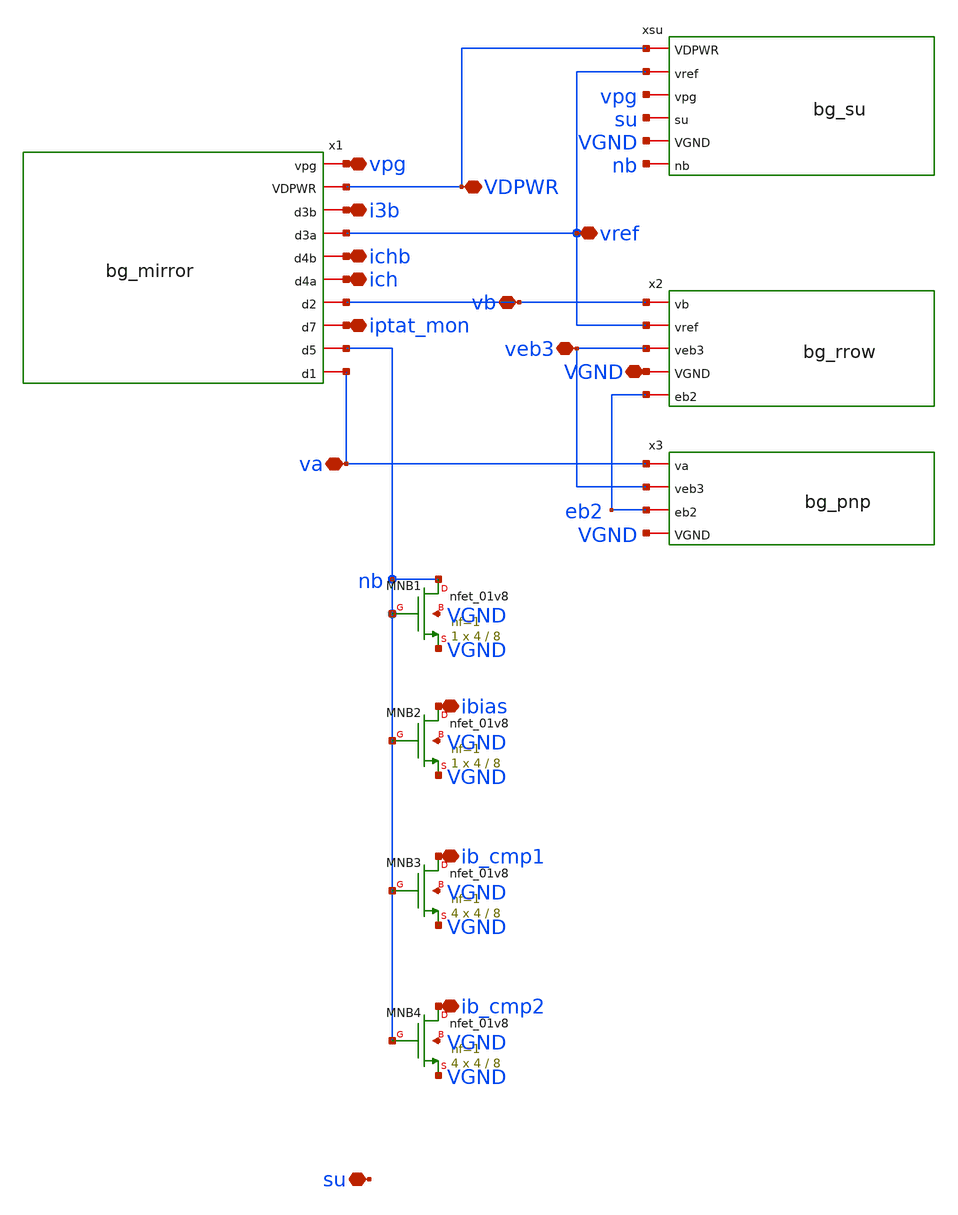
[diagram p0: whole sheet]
** sch_path: xschem/bg_core.sch
**.subckt bg_core va vb vref veb3 vpg i3b VDPWR ichb ich iptat_mon ibias ib_cmp1 ib_cmp2 VGND su
*.iopin va
*.iopin vb
*.iopin vref
*.iopin veb3
*.iopin vpg
*.iopin i3b
*.iopin VDPWR
*.iopin ichb
*.iopin ich
*.iopin iptat_mon
*.iopin ibias
*.iopin ib_cmp1
*.iopin ib_cmp2
*.iopin VGND
*.iopin su
x1 vpg VDPWR i3b vref ichb ich vb iptat_mon nb va bg_mirror
x2 vb vref veb3 VGND eb2 bg_rrow
x3 va veb3 eb2 VGND bg_pnp
XMNB1 nb nb VGND VGND sky130_fd_pr__nfet_01v8 L=8 W=4 nf=1 ad='int((1 + 1)/2) * 4 / 1 * 0.29' as='int((1 + 2)/2) * 4 / 1 * 0.29'
+ pd='2*int((1 + 1)/2) * (4 / 1 + 0.29)' ps='2*int((1 + 2)/2) * (4 / 1 + 0.29)' nrd='0.29 / 4 ' nrs='0.29 / 4 '
+ sa=0 sb=0 sd=0 mult=1 m=1
XMNB2 ibias nb VGND VGND sky130_fd_pr__nfet_01v8 L=8 W=4 nf=1 ad='int((1 + 1)/2) * 4 / 1 * 0.29' as='int((1 + 2)/2) * 4 / 1 * 0.29'
+ pd='2*int((1 + 1)/2) * (4 / 1 + 0.29)' ps='2*int((1 + 2)/2) * (4 / 1 + 0.29)' nrd='0.29 / 4 ' nrs='0.29 / 4 '
+ sa=0 sb=0 sd=0 mult=1 m=1
XMNB3 ib_cmp1 nb VGND VGND sky130_fd_pr__nfet_01v8 L=8 W=4 nf=1 ad='int((1 + 1)/2) * 4 / 1 * 0.29' as='int((1 + 2)/2) * 4 / 1 * 0.29'
+ pd='2*int((1 + 1)/2) * (4 / 1 + 0.29)' ps='2*int((1 + 2)/2) * (4 / 1 + 0.29)' nrd='0.29 / 4 ' nrs='0.29 / 4 '
+ sa=0 sb=0 sd=0 mult=4 m=4
XMNB4 ib_cmp2 nb VGND VGND sky130_fd_pr__nfet_01v8 L=8 W=4 nf=1 ad='int((1 + 1)/2) * 4 / 1 * 0.29' as='int((1 + 2)/2) * 4 / 1 * 0.29'
+ pd='2*int((1 + 1)/2) * (4 / 1 + 0.29)' ps='2*int((1 + 2)/2) * (4 / 1 + 0.29)' nrd='0.29 / 4 ' nrs='0.29 / 4 '
+ sa=0 sb=0 sd=0 mult=4 m=4
xsu VDPWR vref vpg su VGND nb bg_su
**.ends

* expanding   symbol:  bg_mirror.sym # of pins=10
** sym_path: xschem/bg_mirror.sym
** sch_path: xschem/bg_mirror.sch
.subckt bg_mirror vpg VDPWR d3b d3a d4b d4a d2 d7 d5 d1
*.iopin vpg
*.iopin VDPWR
*.iopin d1
*.iopin d2
*.iopin d3a
*.iopin d3b
*.iopin d4a
*.iopin d4b
*.iopin d7
*.iopin d5
XMP1 d1 vpg VDPWR VDPWR sky130_fd_pr__pfet_01v8 L=20 W=8.8 nf=1 ad='int((1 + 1)/2) * 8.8 / 1 * 0.29'
+ as='int((1 + 2)/2) * 8.8 / 1 * 0.29' pd='2*int((1 + 1)/2) * (8.8 / 1 + 0.29)' ps='2*int((1 + 2)/2) * (8.8 / 1 + 0.29)'
+ nrd='0.29 / 8.8 ' nrs='0.29 / 8.8 ' sa=0 sb=0 sd=0 mult=4 m=4
XMP2 d2 vpg VDPWR VDPWR sky130_fd_pr__pfet_01v8 L=20 W=8.8 nf=1 ad='int((1 + 1)/2) * 8.8 / 1 * 0.29'
+ as='int((1 + 2)/2) * 8.8 / 1 * 0.29' pd='2*int((1 + 1)/2) * (8.8 / 1 + 0.29)' ps='2*int((1 + 2)/2) * (8.8 / 1 + 0.29)'
+ nrd='0.29 / 8.8 ' nrs='0.29 / 8.8 ' sa=0 sb=0 sd=0 mult=4 m=4
XMP3A d3a vpg VDPWR VDPWR sky130_fd_pr__pfet_01v8 L=20 W=8.8 nf=1 ad='int((1 + 1)/2) * 8.8 / 1 * 0.29'
+ as='int((1 + 2)/2) * 8.8 / 1 * 0.29' pd='2*int((1 + 1)/2) * (8.8 / 1 + 0.29)' ps='2*int((1 + 2)/2) * (8.8 / 1 + 0.29)'
+ nrd='0.29 / 8.8 ' nrs='0.29 / 8.8 ' sa=0 sb=0 sd=0 mult=2 m=2
XMP3B d3b vpg VDPWR VDPWR sky130_fd_pr__pfet_01v8 L=20 W=8.8 nf=1 ad='int((1 + 1)/2) * 8.8 / 1 * 0.29'
+ as='int((1 + 2)/2) * 8.8 / 1 * 0.29' pd='2*int((1 + 1)/2) * (8.8 / 1 + 0.29)' ps='2*int((1 + 2)/2) * (8.8 / 1 + 0.29)'
+ nrd='0.29 / 8.8 ' nrs='0.29 / 8.8 ' sa=0 sb=0 sd=0 mult=2 m=2
XMP4A d4a vpg VDPWR VDPWR sky130_fd_pr__pfet_01v8 L=20 W=8.8 nf=1 ad='int((1 + 1)/2) * 8.8 / 1 * 0.29'
+ as='int((1 + 2)/2) * 8.8 / 1 * 0.29' pd='2*int((1 + 1)/2) * (8.8 / 1 + 0.29)' ps='2*int((1 + 2)/2) * (8.8 / 1 + 0.29)'
+ nrd='0.29 / 8.8 ' nrs='0.29 / 8.8 ' sa=0 sb=0 sd=0 mult=1 m=1
XMP4B d4b vpg VDPWR VDPWR sky130_fd_pr__pfet_01v8 L=20 W=8.8 nf=1 ad='int((1 + 1)/2) * 8.8 / 1 * 0.29'
+ as='int((1 + 2)/2) * 8.8 / 1 * 0.29' pd='2*int((1 + 1)/2) * (8.8 / 1 + 0.29)' ps='2*int((1 + 2)/2) * (8.8 / 1 + 0.29)'
+ nrd='0.29 / 8.8 ' nrs='0.29 / 8.8 ' sa=0 sb=0 sd=0 mult=1 m=1
XMP7 d7 vpg VDPWR VDPWR sky130_fd_pr__pfet_01v8 L=20 W=8.8 nf=1 ad='int((1 + 1)/2) * 8.8 / 1 * 0.29'
+ as='int((1 + 2)/2) * 8.8 / 1 * 0.29' pd='2*int((1 + 1)/2) * (8.8 / 1 + 0.29)' ps='2*int((1 + 2)/2) * (8.8 / 1 + 0.29)'
+ nrd='0.29 / 8.8 ' nrs='0.29 / 8.8 ' sa=0 sb=0 sd=0 mult=2 m=2
XMP5 d5 vpg VDPWR VDPWR sky130_fd_pr__pfet_01v8 L=20 W=8.8 nf=1 ad='int((1 + 1)/2) * 8.8 / 1 * 0.29'
+ as='int((1 + 2)/2) * 8.8 / 1 * 0.29' pd='2*int((1 + 1)/2) * (8.8 / 1 + 0.29)' ps='2*int((1 + 2)/2) * (8.8 / 1 + 0.29)'
+ nrd='0.29 / 8.8 ' nrs='0.29 / 8.8 ' sa=0 sb=0 sd=0 mult=2 m=2
.ends


* expanding   symbol:  bg_rrow.sym # of pins=5
** sym_path: xschem/bg_rrow.sym
** sch_path: xschem/bg_rrow.sch
.subckt bg_rrow vb vref veb3 VGND eb2
*.iopin vb
*.iopin eb2
*.iopin vref
*.iopin veb3
*.iopin VGND
XR1_1 eb2 net1 VGND sky130_fd_pr__res_high_po_1p41 L=20 mult=1 m=1
XR1_2 net1 net2 VGND sky130_fd_pr__res_high_po_1p41 L=20 mult=1 m=1
XR1_3 net2 net3 VGND sky130_fd_pr__res_high_po_1p41 L=20 mult=1 m=1
XR1_4 net3 vb VGND sky130_fd_pr__res_high_po_1p41 L=20 mult=1 m=1
XR3[39] r3n[38] vref VGND sky130_fd_pr__res_high_po_1p41 L=20 mult=1 m=1
XR3[38] r3n[37] r3n[38] VGND sky130_fd_pr__res_high_po_1p41 L=20 mult=1 m=1
XR3[37] r3n[36] r3n[37] VGND sky130_fd_pr__res_high_po_1p41 L=20 mult=1 m=1
XR3[36] r3n[35] r3n[36] VGND sky130_fd_pr__res_high_po_1p41 L=20 mult=1 m=1
XR3[35] r3n[34] r3n[35] VGND sky130_fd_pr__res_high_po_1p41 L=20 mult=1 m=1
XR3[34] r3n[33] r3n[34] VGND sky130_fd_pr__res_high_po_1p41 L=20 mult=1 m=1
XR3[33] r3n[32] r3n[33] VGND sky130_fd_pr__res_high_po_1p41 L=20 mult=1 m=1
XR3[32] r3n[31] r3n[32] VGND sky130_fd_pr__res_high_po_1p41 L=20 mult=1 m=1
XR3[31] r3n[30] r3n[31] VGND sky130_fd_pr__res_high_po_1p41 L=20 mult=1 m=1
XR3[30] r3n[29] r3n[30] VGND sky130_fd_pr__res_high_po_1p41 L=20 mult=1 m=1
XR3[29] r3n[28] r3n[29] VGND sky130_fd_pr__res_high_po_1p41 L=20 mult=1 m=1
XR3[28] r3n[27] r3n[28] VGND sky130_fd_pr__res_high_po_1p41 L=20 mult=1 m=1
XR3[27] r3n[26] r3n[27] VGND sky130_fd_pr__res_high_po_1p41 L=20 mult=1 m=1
XR3[26] r3n[25] r3n[26] VGND sky130_fd_pr__res_high_po_1p41 L=20 mult=1 m=1
XR3[25] r3n[24] r3n[25] VGND sky130_fd_pr__res_high_po_1p41 L=20 mult=1 m=1
XR3[24] r3n[23] r3n[24] VGND sky130_fd_pr__res_high_po_1p41 L=20 mult=1 m=1
XR3[23] r3n[22] r3n[23] VGND sky130_fd_pr__res_high_po_1p41 L=20 mult=1 m=1
XR3[22] r3n[21] r3n[22] VGND sky130_fd_pr__res_high_po_1p41 L=20 mult=1 m=1
XR3[21] r3n[20] r3n[21] VGND sky130_fd_pr__res_high_po_1p41 L=20 mult=1 m=1
XR3[20] r3n[19] r3n[20] VGND sky130_fd_pr__res_high_po_1p41 L=20 mult=1 m=1
XR3[19] r3n[18] r3n[19] VGND sky130_fd_pr__res_high_po_1p41 L=20 mult=1 m=1
XR3[18] r3n[17] r3n[18] VGND sky130_fd_pr__res_high_po_1p41 L=20 mult=1 m=1
XR3[17] r3n[16] r3n[17] VGND sky130_fd_pr__res_high_po_1p41 L=20 mult=1 m=1
XR3[16] r3n[15] r3n[16] VGND sky130_fd_pr__res_high_po_1p41 L=20 mult=1 m=1
XR3[15] r3n[14] r3n[15] VGND sky130_fd_pr__res_high_po_1p41 L=20 mult=1 m=1
XR3[14] r3n[13] r3n[14] VGND sky130_fd_pr__res_high_po_1p41 L=20 mult=1 m=1
XR3[13] r3n[12] r3n[13] VGND sky130_fd_pr__res_high_po_1p41 L=20 mult=1 m=1
XR3[12] r3n[11] r3n[12] VGND sky130_fd_pr__res_high_po_1p41 L=20 mult=1 m=1
XR3[11] r3n[10] r3n[11] VGND sky130_fd_pr__res_high_po_1p41 L=20 mult=1 m=1
XR3[10] r3n[9] r3n[10] VGND sky130_fd_pr__res_high_po_1p41 L=20 mult=1 m=1
XR3[9] r3n[8] r3n[9] VGND sky130_fd_pr__res_high_po_1p41 L=20 mult=1 m=1
XR3[8] r3n[7] r3n[8] VGND sky130_fd_pr__res_high_po_1p41 L=20 mult=1 m=1
XR3[7] r3n[6] r3n[7] VGND sky130_fd_pr__res_high_po_1p41 L=20 mult=1 m=1
XR3[6] r3n[5] r3n[6] VGND sky130_fd_pr__res_high_po_1p41 L=20 mult=1 m=1
XR3[5] r3n[4] r3n[5] VGND sky130_fd_pr__res_high_po_1p41 L=20 mult=1 m=1
XR3[4] r3n[3] r3n[4] VGND sky130_fd_pr__res_high_po_1p41 L=20 mult=1 m=1
XR3[3] r3n[2] r3n[3] VGND sky130_fd_pr__res_high_po_1p41 L=20 mult=1 m=1
XR3[2] r3n[1] r3n[2] VGND sky130_fd_pr__res_high_po_1p41 L=20 mult=1 m=1
XR3[1] r3n[0] r3n[1] VGND sky130_fd_pr__res_high_po_1p41 L=20 mult=1 m=1
XR3[0] veb3 r3n[0] VGND sky130_fd_pr__res_high_po_1p41 L=20 mult=1 m=1
XRD[3] VGND VGND VGND sky130_fd_pr__res_high_po_1p41 L=20 mult=1 m=1
XRD[2] VGND VGND VGND sky130_fd_pr__res_high_po_1p41 L=20 mult=1 m=1
XRD[1] VGND VGND VGND sky130_fd_pr__res_high_po_1p41 L=20 mult=1 m=1
XRD[0] VGND VGND VGND sky130_fd_pr__res_high_po_1p41 L=20 mult=1 m=1
.ends


* expanding   symbol:  bg_pnp.sym # of pins=4
** sym_path: xschem/bg_pnp.sym
** sch_path: xschem/bg_pnp.sch
.subckt bg_pnp va veb3 eb2 VGND
*.iopin va
*.iopin eb2
*.iopin veb3
*.iopin VGND
XQ1 VGND VGND va sky130_fd_pr__pnp_05v5_W3p40L3p40 m=1
XQ2 VGND VGND eb2 sky130_fd_pr__pnp_05v5_W3p40L3p40 m=8
XQ3 VGND VGND veb3 sky130_fd_pr__pnp_05v5_W3p40L3p40 m=1
XQD VGND VGND VGND sky130_fd_pr__pnp_05v5_W3p40L3p40 m=15
.ends


* expanding   symbol:  bg_su.sym # of pins=6
** sym_path: xschem/bg_su.sym
** sch_path: xschem/bg_su.sch
.subckt bg_su VDPWR vref vpg su VGND nb
*.iopin vref
*.iopin VGND
*.iopin vpg
*.iopin VDPWR
*.iopin su
*.iopin nb
XMSU1 su vref VDPWR VDPWR sky130_fd_pr__pfet_01v8 L=20 W=0.42 nf=1 ad='int((1 + 1)/2) * 0.42 / 1 * 0.29'
+ as='int((1 + 2)/2) * 0.42 / 1 * 0.29' pd='2*int((1 + 1)/2) * (0.42 / 1 + 0.29)' ps='2*int((1 + 2)/2) * (0.42 / 1 + 0.29)'
+ nrd='0.29 / 0.42 ' nrs='0.29 / 0.42 ' sa=0 sb=0 sd=0 mult=1 m=1
XMSU3 su nb VGND VGND sky130_fd_pr__nfet_01v8 L=1 W=0.42 nf=1 ad='int((1 + 1)/2) * 0.42 / 1 * 0.29' as='int((1 + 2)/2) * 0.42 / 1 * 0.29'
+ pd='2*int((1 + 1)/2) * (0.42 / 1 + 0.29)' ps='2*int((1 + 2)/2) * (0.42 / 1 + 0.29)' nrd='0.29 / 0.42 '
+ nrs='0.29 / 0.42 ' sa=0 sb=0 sd=0 mult=1 m=1
XMSU2 vpg su VGND VGND sky130_fd_pr__nfet_01v8 L=10 W=0.42 nf=1 ad='int((1 + 1)/2) * 0.42 / 1 * 0.29'
+ as='int((1 + 2)/2) * 0.42 / 1 * 0.29' pd='2*int((1 + 1)/2) * (0.42 / 1 + 0.29)' ps='2*int((1 + 2)/2) * (0.42 / 1 + 0.29)'
+ nrd='0.29 / 0.42 ' nrs='0.29 / 0.42 ' sa=0 sb=0 sd=0 mult=1 m=1
.ends

.end
